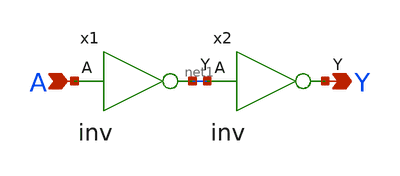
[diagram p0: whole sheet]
** sch_path: design/xschem/INV/buffer.sch
**.subckt buffer A Y
*.ipin A
*.opin Y
x1 A VSS VDD net1 inv
x2 net1 VSS VDD Y inv
**.ends

* expanding   symbol:  INV/inv.sym # of pins=2
** sym_path: design/xschem/INV/inv.sym
** sch_path: design/xschem/INV/inv.sch
.subckt inv A VSS VDD Y
*.ipin A
*.opin Y
XM2 Y A VSS GND sky130_fd_pr__nfet_01v8 L=0.15 W=1 nf=1 ad='int((nf+1)/2) * W/nf * 0.29' as='int((nf+2)/2) * W/nf * 0.29'
+ pd='2*int((nf+1)/2) * (W/nf + 0.29)' ps='2*int((nf+2)/2) * (W/nf + 0.29)' nrd='0.29 / W' nrs='0.29 / W'
+ sa=0 sb=0 sd=0 mult=1 m=1
XM1 Y A VDD VDD sky130_fd_pr__pfet_01v8 L=0.15 W=3.21 nf=1 ad='int((nf+1)/2) * W/nf * 0.29' as='int((nf+2)/2) * W/nf * 0.29'
+ pd='2*int((nf+1)/2) * (W/nf + 0.29)' ps='2*int((nf+2)/2) * (W/nf + 0.29)' nrd='0.29 / W' nrs='0.29 / W'
+ sa=0 sb=0 sd=0 mult=1 m=1
.ends

.end
